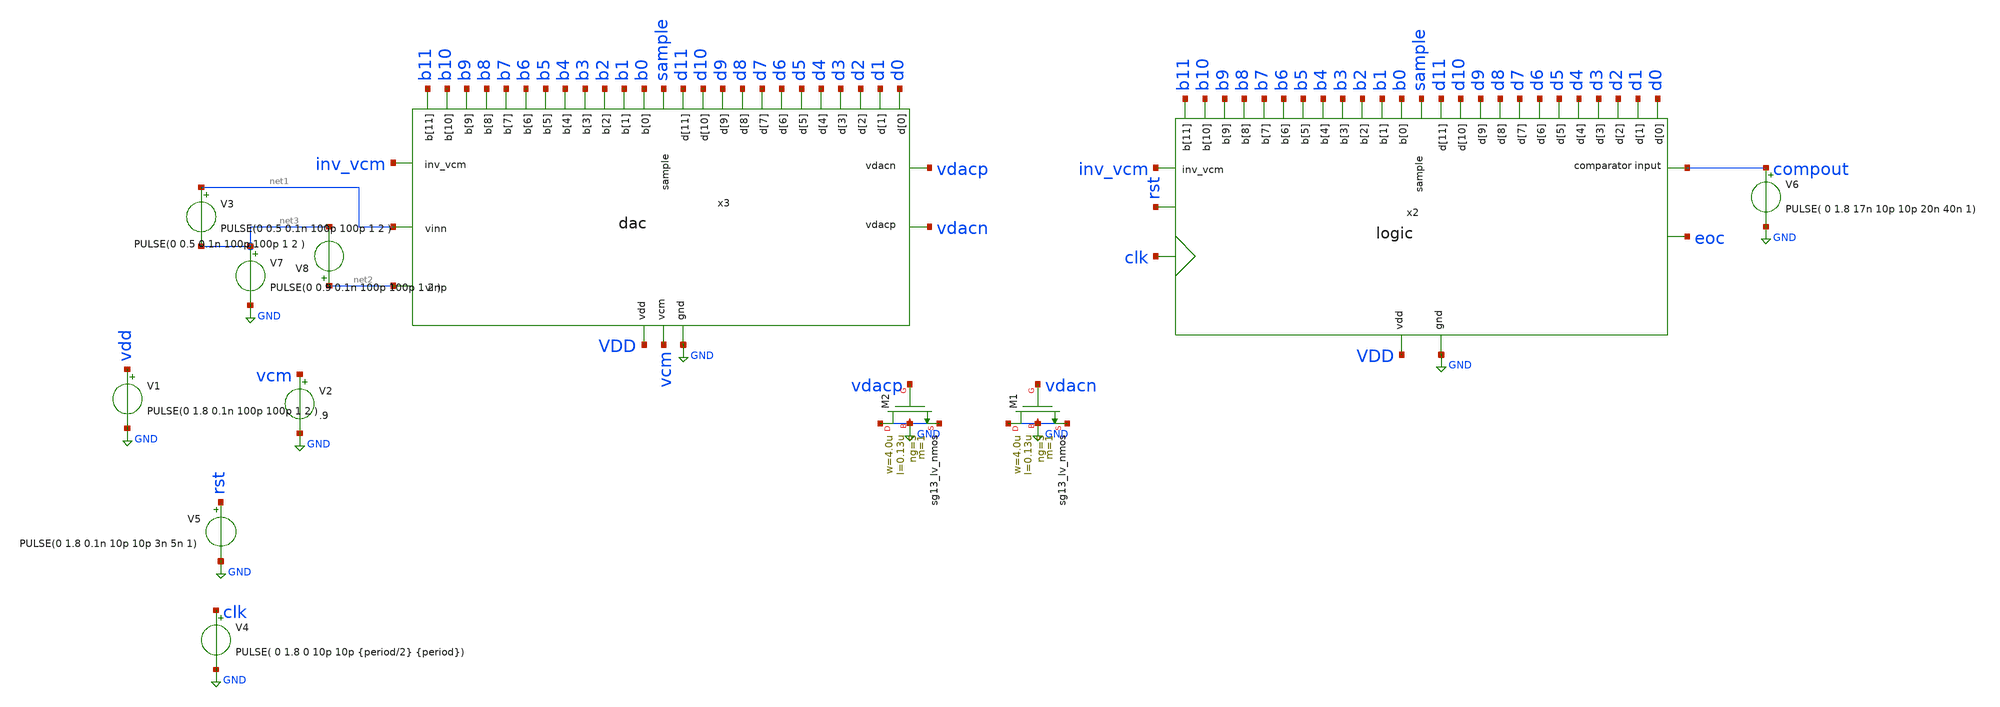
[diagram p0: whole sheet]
** sch_path: xschem/dac_icms_cell/testbenches/tb_dac.sch
**.subckt tb_dac
x3 vdacp vcm b9 b7 b0 b11 b3 b4 b2 b1 b8 b6 b5 b10 GND VDD sample vdacn net2 net1 d9 d7 d0 d11 d3 d4
+ d2 d1 d8 d6 d5 d10 inv_vcm dac cu=10f
V2 vcm GND .9
x2 b9 b7 b0 b11 b3 b4 b2 b1 b8 b6 b5 b10 GND VDD sample d9 d7 d0 d11 d3 d4 d2 d1 d8 d6 d5 d10
+ compout clk rst eoc inv_vcm logic
V4 clk GND PULSE( 0 1.8 0 10p 10p {period/2} {period})
V5 rst GND PULSE(0 1.8 0.1n 10p 10p 3n 5n 1)
XM2 GND vdacp GND GND sg13_lv_nmos w=4.0u l=0.13u ng=5 m=1 mm_ok=1
XM1 GND vdacn GND GND sg13_lv_nmos w=4.0u l=0.13u ng=5 m=1 mm_ok=1
V6 compout GND PULSE( 0 1.8 17n 10p 10p 20n 40n 1)
V1 vdd GND PULSE(0 1.8 0.1n 100p 100p 1 2 )
V7 net3 GND PULSE(0 0.9 0.1n 100p 100p 1 2 )
V3 net1 net3 PULSE(0 0.5 0.1n 100p 100p 1 2 )
V8 net2 net3 PULSE(0 0.5 0.1n 100p 100p 1 2 )
**** begin user architecture code


.param temp=27
.param period = 2n
.param stop={15*period}
.param ro = 500
.param W_P = 1.0u
.param L_P = 0.13u
.param W_N = 1.0u
.param L_N = 0.13u
.options savecurrents klu method=gear reltol=1e-2 abstol=1e-10 gmin=1e-10
.control

* Transient Analysis
tran 200p 30n
*Busco los valores finales de cdacp y cdacn
meas tran tstart when sample=0.18 fall=1
meas tran valor_s_p find vdacp when clk=0.18 td=$&tstart fall=1
meas tran valor_1_p find vdacp when clk=0.18 td=$&tstart fall=2
meas tran valor_2_p find vdacp when clk=0.18 td=$&tstart fall=3
meas tran valor_3_p find vdacp when clk=0.18 td=$&tstart fall=4
meas tran valor_4_p find vdacp when clk=0.18 td=$&tstart fall=5
meas tran valor_5_p find vdacp when clk=0.18 td=$&tstart fall=6
meas tran valor_6_p find vdacp when clk=0.18 td=$&tstart fall=7
meas tran valor_7_p find vdacp when clk=0.18 td=$&tstart fall=8
meas tran valor_8_p find vdacp when clk=0.18 td=$&tstart fall=9
meas tran valor_9_p find vdacp when clk=0.18 td=$&tstart fall=10
meas tran valor_10_p find vdacp when clk=0.18 td=$&tstart fall=11
meas tran valor_11_p find vdacp when clk=0.18 td=$&tstart fall=12

meas tran valor_s_n find vdacn when clk=0.18 td=$&tstart fall=1
meas tran valor_1_n find vdacn when clk=0.18 td=$&tstart fall=2
meas tran valor_2_n find vdacn when clk=0.18 td=$&tstart fall=3
meas tran valor_3_n find vdacn when clk=0.18 td=$&tstart fall=4
meas tran valor_4_n find vdacn when clk=0.18 td=$&tstart fall=5
meas tran valor_5_n find vdacn when clk=0.18 td=$&tstart fall=6
meas tran valor_6_n find vdacn when clk=0.18 td=$&tstart fall=7
meas tran valor_7_n find vdacn when clk=0.18 td=$&tstart fall=8
meas tran valor_8_n find vdacn when clk=0.18 td=$&tstart fall=9
meas tran valor_9_n find vdacn when clk=0.18 td=$&tstart fall=10
meas tran valor_10_n find vdacn when clk=0.18 td=$&tstart fall=11
meas tran valor_11_n find vdacn when clk=0.18 td=$&tstart fall=12

*Calculo los valores de la señal diferencial (vdacd)

let vdacds=valor_s_p-valor_s_n
let vdacd1 = valor_1_p-valor_1_n
let vdacd2 = valor_2_p-valor_2_n
let vdacd3 = valor_3_p-valor_3_n
let vdacd4 = valor_4_p-valor_4_n
let vdacd5 = valor_5_p-valor_5_n
let vdacd6 = valor_6_p-valor_6_n
let vdacd7 = valor_7_p - valor_7_n
let vdacd8 = valor_8_p - valor_8_n
let vdacd9 = valor_9_p - valor_9_n
let vdacd10 = valor_10_p - valor_10_n
let vdacd11 = valor_11_p - valor_11_n

*Calculo los saltos tanto del lado p como del n
let salto1p = valor_1_p-valor_s_p
let salto2p = valor_2_p-valor_1_p
let salto3p = valor_3_p-valor_2_p
let salto4p = valor_4_p-valor_3_p
let salto5p = valor_5_p-valor_4_p
let salto6p = valor_6_p-valor_5_p
let salto7p = valor_7_p-valor_6_p
let salto8p = valor_8_p-valor_7_p
let salto9p = valor_9_p-valor_8_p
let salto10p = valor_10_p-valor_9_p
let salto11p = valor_11_p-valor_10_p


let salto1n = valor_1_n-valor_s_n
let salto2n = valor_2_n-valor_1_n
let salto3n = valor_3_n-valor_2_n
let salto4n = valor_4_n-valor_3_n
let salto5n = valor_5_n-valor_4_n
let salto6n = valor_6_n-valor_5_n
let salto7n = valor_7_n-valor_6_n
let salto8n = valor_8_n-valor_7_n
let salto9n = valor_9_n-valor_8_n
let salto10n = valor_10_n-valor_9_n
let salto11n = valor_11_n-valor_10_n


let salto1 = vdacd1-vdacds
let salto2 = vdacd2-vdacd1
let salto3 = vdacd3-vdacd2
let salto4 = vdacd4-vdacd3
let salto5 = vdacd5-vdacd4
let salto6 = vdacd6-vdacd5
let salto7 = vdacd7 - vdacd6
let salto8 = vdacd8 - vdacd7
let salto9 = vdacd9 - vdacd8
let salto10 = vdacd10 - vdacd9
let salto11 = vdacd11 - vdacd10


echo Sample VdacP $&valor_s_p VdacN $&valor_s_n Vdac diff $&vdacds
echo Salto 1 VdacP $&salto1p VdacN $&salto1n Vdac diff $&salto1
echo Salto 2 VdacP $&salto2p VdacN $&salto2n Vdac diff $&salto2
echo Salto 3 VdacP $&salto3p VdacN $&salto3n Vdac diff $&salto3
echo Salto 4 VdacP $&salto4p VdacN $&salto4n Vdac diff $&salto4
echo Salto 5 VdacP $&salto5p VdacN $&salto5n Vdac diff $&salto5
echo Salto 6 VdacP $&salto6p VdacN $&salto6n Vdac diff $&salto6
echo Salto 7 VdacP $&salto7p VdacN $&salto7n Vdac diff $&salto7
echo Salto 8 VdacP $&salto8p VdacN $&salto8n Vdac diff $&salto8
echo Salto 9 VdacP $&salto9p VdacN $&salto9n Vdac diff $&salto9
echo Salto 10 VdacP $&salto10p VdacN $&salto10n Vdac diff $&salto10
echo Salto 11 VdacP $&salto11p VdacN $&salto11n Vdac diff $&salto11

let sigvalor1p= {0.9*salto1p+valor_s_p}
let sigvalor2p= {0.9*salto2p+valor_1_p}
let sigvalor3p= {0.9*salto3p+valor_2_p}
let sigvalor4p= {0.9*salto4p+valor_3_p}
let sigvalor5p= {0.9*salto5p+valor_4_p}
let sigvalor6p= {0.9*salto6p+valor_5_p}
let sigvalor7p= {0.9*salto7p+valor_6_p}
let sigvalor8p= {0.9*salto8p+valor_7_p}
let sigvalor9p= {0.9*salto9p+valor_8_p}
let sigvalor10p= {0.9*salto10p+valor_9_p}
let sigvalor11p= {0.9*salto11p+valor_10_p}


let sigvalor1n= {0.9*salto1n+valor_s_n}
let sigvalor2n= {0.9*salto2n+valor_1_n}
let sigvalor3n= {0.9*salto3n+valor_2_n}
let sigvalor4n= {0.9*salto4n+valor_3_n}
let sigvalor5n= {0.9*salto5n+valor_4_n}
let sigvalor6n= {0.9*salto6n+valor_5_n}
let sigvalor7n= {0.9*salto7n+valor_6_n}
let sigvalor8n= {0.9*salto8n+valor_7_n}
let sigvalor9n= {0.9*salto9n+valor_8_n}
let sigvalor10n= {0.9*salto10n+valor_9_n}
let sigvalor11n= {0.9*salto11n+valor_10_n}

let sigvalor_s_p = {0.9*(valor_s_p-0.9) + 0.9}
let sigvalor_s_n = {0.9*(valor_s_n-0.9) + 0.9}

meas tran t_sett_sample_p trig at=$&tstart targ vdacp val=$&sigvalor_s_p cross=1 from=3n
meas tran t_sett_sample_n trig at=$&tstart targ vdacn val=$&sigvalor_s_n cross=1 from=3n

meas tran t_sett_1_p trig clk val=1.62 rise=1 targ vdacp val=$&sigvalor1p cross=1 from=5n
meas tran t_sett_2_p trig clk val=1.62 rise=2 targ vdacp val=$&sigvalor2p cross=1 from=5n
meas tran t_sett_3_p trig clk val=1.62 rise=3 targ vdacp val=$&sigvalor3p cross=1 from=5n
meas tran t_sett_4_p trig clk val=1.62 rise=4 targ vdacp val=$&sigvalor4p cross=1 from=5n
meas tran t_sett_5_p trig clk val=1.62 rise=5 targ vdacp val=$&sigvalor5p cross=1 from=5n
meas tran t_sett_6_p trig clk val=1.62 rise=6 targ vdacp val=$&sigvalor6p cross=1 from=5n
meas tran t_sett_7_p trig clk val=1.62 rise=7 targ vdacp val=$&sigvalor7p cross=1 from=5n
meas tran t_sett_8_p trig clk val=1.62 rise=8 targ vdacp val=$&sigvalor8p cross=1 from=5n
meas tran t_sett_9_p trig clk val=1.62 rise=9 targ vdacp val=$&sigvalor9p cross=1 from=5n
meas tran t_sett_10_p trig clk val=1.62 rise=10 targ vdacp val=$&sigvalor10p cross=1 from=5n
meas tran t_sett_11_p trig clk val=1.62 rise=11 targ vdacp val=$&sigvalor11p cross=1 from=5n


meas tran t_sett_1_n trig clk val=1.62 rise=1 targ vdacn val=$&sigvalor1n cross=1 from=5n
meas tran t_sett_2_n trig clk val=1.62 rise=2 targ vdacn val=$&sigvalor2n cross=1 from=5n
meas tran t_sett_3_n trig clk val=1.62 rise=3 targ vdacn val=$&sigvalor3n cross=1 from=5n
meas tran t_sett_4_n trig clk val=1.62 rise=4 targ vdacn val=$&sigvalor4n cross=1 from=5n
meas tran t_sett_5_n trig clk val=1.62 rise=5 targ vdacn val=$&sigvalor5n cross=1 from=5n
meas tran t_sett_6_n trig clk val=1.62 rise=6 targ vdacn val=$&sigvalor6n cross=1 from=5n
meas tran t_sett_7_n trig clk val=1.62 rise=7 targ vdacn val=$&sigvalor7n cross=1 from=5n
meas tran t_sett_8_n trig clk val=1.62 rise=8 targ vdacn val=$&sigvalor8n cross=1 from=5n
meas tran t_sett_9_n trig clk val=1.62 rise=9 targ vdacn val=$&sigvalor9n cross=1 from=5n
meas tran t_sett_10_n trig clk val=1.62 rise=10 targ vdacn val=$&sigvalor10n cross=1 from=5n
meas tran t_sett_11_n trig clk val=1.62 rise=11 targ vdacn val=$&sigvalor11n cross=1 from=5n



plot {d0} {d1 + 4} {d2 + 8} {d3 + 12} {d4 + 16} {d5 + 20} {d6 + 24} {d7 + 28} {d8 + 32} {d9 + 36} {d10 + 40}
+ {d11 + 44}
plot {b0} {b1 + 4} {b2 + 8} {b3 + 12} {b4 + 16} {b5 + 20} {b6 + 24} {b7 + 28} {b8 + 32} {b9 + 36} {b10 + 40}
+ {b11 + 44}
plot {clk} {comp_in + 2} {sample + 4}
plot vdacp vdacn
plot {vdacp-vdacn}
plot x3.vdacp2 x3.vdacn2 compout

.endc




** IHP models
.lib cornerMOSlv.lib mos_ss
.lib cornerMOShv.lib mos_tt
.lib cornerHBT.lib hbt_typ
.lib cornerRES.lib res_typ
.lib cornerCAP.lib cap_typ
.include /foss/pdks/ihp-sg13g2/libs.ref/sg13g2_stdcell/spice/sg13g2_stdcell.spice


**** end user architecture code
**.ends
.GLOBAL GND
.end
